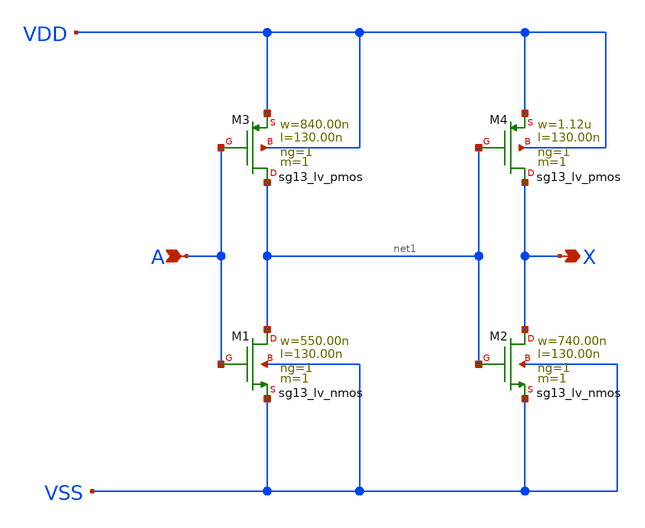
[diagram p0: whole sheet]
** sch_path: ihp-sg13g2/libs.ref/sg13g2_stdcell/sch/xschem/sg13g2_buf_1.sch
* Copyright 2023 IHP PDK Authors
* Licensed under the Apache License, Version 2.0 (the "License");
* you may not use this file except in compliance with the License.
* You may obtain a copy of the License at
* https://www.apache.org/licenses/LICENSE-2.0
* Unless required by applicable law or agreed to in writing, software
* distributed under the License is distributed on an "AS IS" BASIS,
* WITHOUT WARRANTIES OR CONDITIONS OF ANY KIND, either express or implied.
* See the License for the specific language governing permissions and
* limitations under the License.
**.subckt sg13g2_buf_1 A X
*.ipin A
*.opin X
XM1 net1 A VSS VSS sg13_lv_nmos w=550.00n l=130.00n ng=1 m=1 mm_ok=1
XM2 X net1 VSS VSS sg13_lv_nmos w=740.00n l=130.00n ng=1 m=1 mm_ok=1
XM3 net1 A VDD VDD sg13_lv_pmos w=840.00n l=130.00n ng=1 m=1 mm_ok=1
XM4 X net1 VDD VDD sg13_lv_pmos w=1.12u l=130.00n ng=1 m=1 mm_ok=1
**.ends
.end
